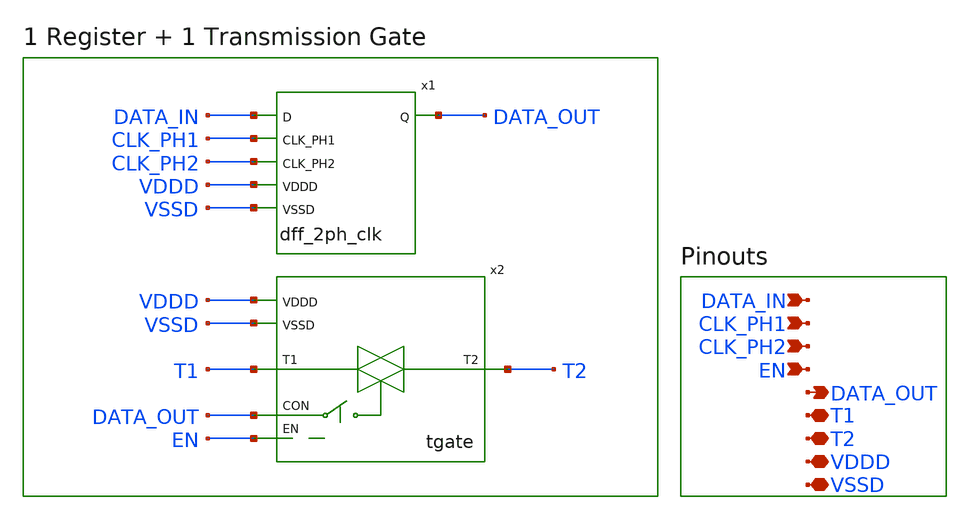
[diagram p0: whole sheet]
** sch_path: designs/libs/core_switch_matrix/switch_cell/switch_cell.sch
**.subckt switch_cell DATA_IN CLK_PH1 CLK_PH2 DATA_OUT VDDD VSSD EN T1 T2
*.ipin DATA_IN
*.ipin CLK_PH1
*.ipin CLK_PH2
*.opin DATA_OUT
*.iopin VDDD
*.iopin VSSD
*.ipin EN
*.iopin T1
*.iopin T2
x1 DATA_IN CLK_PH1 CLK_PH2 DATA_OUT VDDD VSSD dff_2ph_clk
x2 DATA_OUT EN VDDD VSSD T1 T2 tgate
**.ends

* expanding   symbol:  libs/core_switch_matrix/dff_2ph_clk/dff_2ph_clk.sym # of pins=6
** sym_path: designs/libs/core_switch_matrix/dff_2ph_clk/dff_2ph_clk.sym
** sch_path: designs/libs/core_switch_matrix/dff_2ph_clk/dff_2ph_clk.sch
.subckt dff_2ph_clk D CLK_PH1 CLK_PH2 Q VDDD VSSD
*.ipin D
*.ipin CLK_PH1
*.ipin CLK_PH2
*.opin Q
*.iopin VDDD
*.iopin VSSD
x1 D CLK_PH1 net1 VDDD VDDD VSSD VSSD gf180mcu_fd_sc_mcu9t5v0__latq_1
x2 net1 CLK_PH2 Q VDDD VDDD VSSD VSSD gf180mcu_fd_sc_mcu9t5v0__latq_1
**** begin user architecture code

.include /foss/pdks/gf180mcuD/libs.ref/gf180mcu_fd_sc_mcu9t5v0/spice/gf180mcu_fd_sc_mcu9t5v0.spice

**** end user architecture code
.ends


* expanding   symbol:  libs/core_switch_matrix/tgate/tgate.sym # of pins=6
** sym_path: designs/libs/core_switch_matrix/tgate/tgate.sym
** sch_path: designs/libs/core_switch_matrix/tgate/tgate.sch
.subckt tgate CON EN VDDD VSSD T1 T2
*.ipin CON
*.ipin EN
*.iopin VDDD
*.iopin VSSD
*.iopin T1
*.iopin T2
XM1 T2 NCON T1 VSSD nfet_03v3 L=0.28u W=4u nf=1 ad='int((nf+1)/2) * W/nf * 0.18u' as='int((nf+2)/2) * W/nf * 0.18u'
+ pd='2*int((nf+1)/2) * (W/nf + 0.18u)' ps='2*int((nf+2)/2) * (W/nf + 0.18u)' nrd='0.18u / W' nrs='0.18u / W'
+ sa=0 sb=0 sd=0 m=6
XM2 T2 PCON T1 VDDD pfet_03v3 L=0.28u W=4u nf=1 ad='int((nf+1)/2) * W/nf * 0.18u' as='int((nf+2)/2) * W/nf * 0.18u'
+ pd='2*int((nf+1)/2) * (W/nf + 0.18u)' ps='2*int((nf+2)/2) * (W/nf + 0.18u)' nrd='0.18u / W' nrs='0.18u / W'
+ sa=0 sb=0 sd=0 m=18
x1 CON EN VSSD VDDD VSSD VDDD net1 gf180mcu_fd_sc_mcu9t5v0__nand2_1
x2 net1 VSSD VDDD VSSD VDDD NCON gf180mcu_fd_sc_mcu9t5v0__inv_1
x3 NCON VSSD VDDD VSSD VDDD PCON gf180mcu_fd_sc_mcu9t5v0__inv_1
**** begin user architecture code

.include /foss/pdks/gf180mcuD/libs.ref/gf180mcu_fd_sc_mcu9t5v0/spice/gf180mcu_fd_sc_mcu9t5v0.spice

**** end user architecture code
.ends

.end
